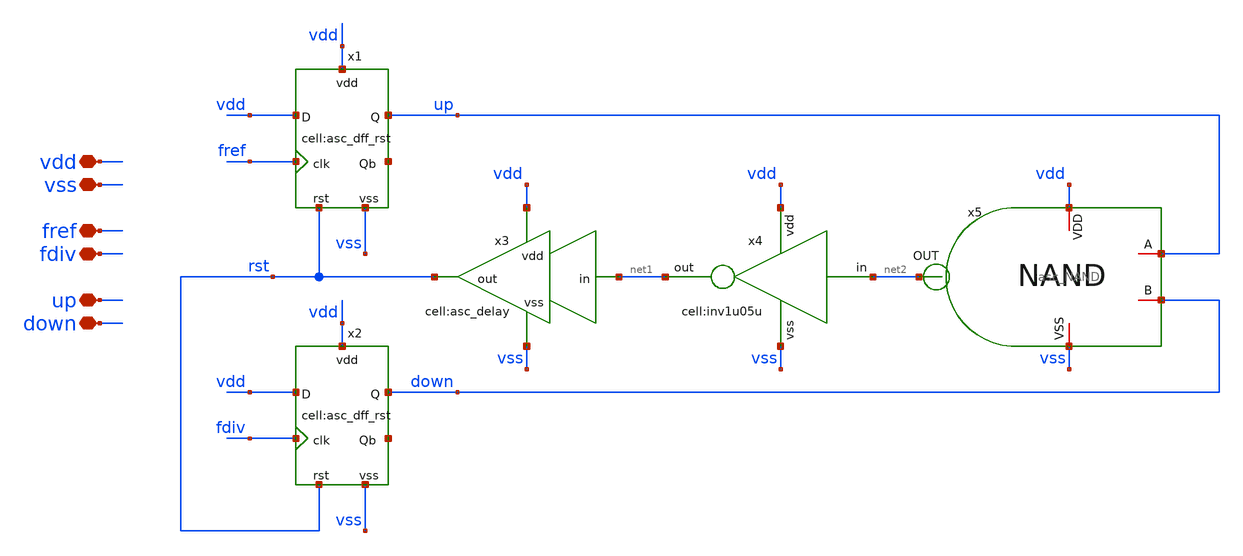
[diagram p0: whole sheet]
** sch_path: designs/libs/xp_core_analog/asc_PFD_DFF/asc_PFD_DFF.sch
**.subckt asc_PFD_DFF vdd vss fref fdiv up down
*.iopin vdd
*.iopin vss
*.iopin fref
*.iopin fdiv
*.iopin up
*.iopin down
x1 fref vdd net3 vdd vss up rst asc_dff_rst
x2 fdiv vdd net4 vdd vss down rst asc_dff_rst
x4 net2 vdd net1 vss inv1u05u
x3 net1 vss rst vdd asc_delay
x5 vdd net2 up down vss asc_NAND
**.ends
.end
